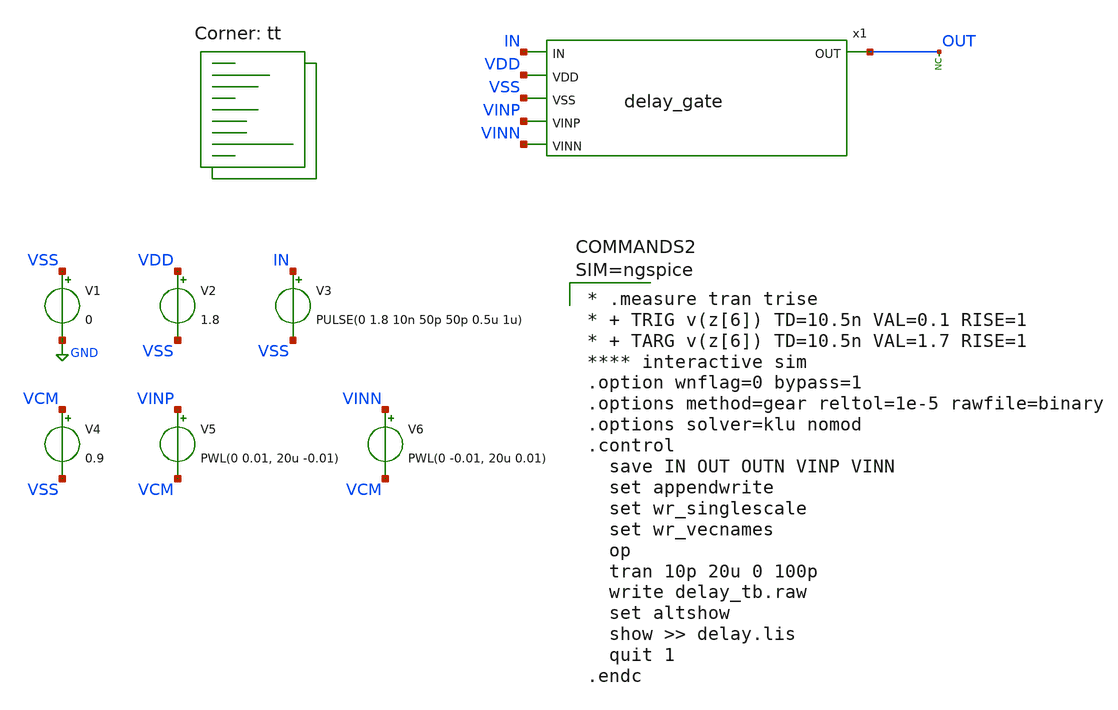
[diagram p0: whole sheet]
** sch_path: xschem/delay_tb.sch
.include $::SKYWATER_STDCELLS/sky130_fd_sc_hd.spice
**.subckt delay_tb
x1 IN VDD VSS VINP VINN OUT delay_gate
V1 VSS GND 0
V2 VDD VSS 1.8
V3 IN VSS PULSE(0 1.8 10n 50p 50p 0.5u 1u)
V4 VCM VSS 0.9
V5 VINP VCM PWL(0 0.01, 20u -0.01)
V6 VINN VCM PWL(0 -0.01, 20u 0.01)
* noconn OUT
**** begin user architecture code
.lib $::SKYWATER_MODELS/sky130.lib.spice tt


* .measure tran trise
* + TRIG v(z[6]) TD=10.5n VAL=0.1 RISE=1
* + TARG v(z[6]) TD=10.5n VAL=1.7 RISE=1
**** interactive sim
.option wnflag=0 bypass=1
.options method=gear reltol=1e-5 rawfile=binary
.options solver=klu nomod
.control
  save IN OUT OUTN VINP VINN
  set appendwrite
  set wr_singlescale
  set wr_vecnames
  op
  tran 10p 20u 0 100p
  write delay_tb.raw
  set altshow
  show >> delay.lis
  quit 1
.endc



**** end user architecture code
**.ends

* expanding   symbol:  delay_gate.sym # of pins=6
** sym_path: xschem/delay_gate.sym
** sch_path: xschem/delay_gate.sch
.subckt delay_gate IN VDD VSS VINP VINN OUT
*.ipin VINP
*.ipin VINN
*.ipin IN
*.ipin VSS
*.ipin VDD
*.opin OUT
XM1 net3 VINP net8 VDD sky130_fd_pr__pfet_01v8 L=1 W=3 nf=1 ad='int((nf+1)/2) * W/nf * 0.29' as='int((nf+2)/2) * W/nf * 0.29'
+ pd='2*int((nf+1)/2) * (W/nf + 0.29)' ps='2*int((nf+2)/2) * (W/nf + 0.29)' nrd='0.29 / W' nrs='0.29 / W'
+ sa=0 sb=0 sd=0 mult=1 m=1
XM2 net2 net1 net3 VDD sky130_fd_pr__pfet_01v8 L=1 W=3 nf=1 ad='int((nf+1)/2) * W/nf * 0.29' as='int((nf+2)/2) * W/nf * 0.29'
+ pd='2*int((nf+1)/2) * (W/nf + 0.29)' ps='2*int((nf+2)/2) * (W/nf + 0.29)' nrd='0.29 / W' nrs='0.29 / W'
+ sa=0 sb=0 sd=0 mult=1 m=1
XM3 net2 net1 net6 VSS sky130_fd_pr__nfet_01v8 L=1 W=1 nf=1 ad='int((nf+1)/2) * W/nf * 0.29' as='int((nf+2)/2) * W/nf * 0.29'
+ pd='2*int((nf+1)/2) * (W/nf + 0.29)' ps='2*int((nf+2)/2) * (W/nf + 0.29)' nrd='0.29 / W' nrs='0.29 / W'
+ sa=0 sb=0 sd=0 mult=1 m=1
XM4 net1 IN net5 VDD sky130_fd_pr__pfet_01v8 L=1 W=3 nf=1 ad='int((nf+1)/2) * W/nf * 0.29' as='int((nf+2)/2) * W/nf * 0.29'
+ pd='2*int((nf+1)/2) * (W/nf + 0.29)' ps='2*int((nf+2)/2) * (W/nf + 0.29)' nrd='0.29 / W' nrs='0.29 / W'
+ sa=0 sb=0 sd=0 mult=1 m=1
XM5 net1 IN net4 VSS sky130_fd_pr__nfet_01v8 L=1 W=1 nf=1 ad='int((nf+1)/2) * W/nf * 0.29' as='int((nf+2)/2) * W/nf * 0.29'
+ pd='2*int((nf+1)/2) * (W/nf + 0.29)' ps='2*int((nf+2)/2) * (W/nf + 0.29)' nrd='0.29 / W' nrs='0.29 / W'
+ sa=0 sb=0 sd=0 mult=1 m=1
XM6 net4 VINN net7 VSS sky130_fd_pr__nfet_01v8 L=1 W=1 nf=1 ad='int((nf+1)/2) * W/nf * 0.29' as='int((nf+2)/2) * W/nf * 0.29'
+ pd='2*int((nf+1)/2) * (W/nf + 0.29)' ps='2*int((nf+2)/2) * (W/nf + 0.29)' nrd='0.29 / W' nrs='0.29 / W'
+ sa=0 sb=0 sd=0 mult=1 m=1
x6 net2 VSS VSS VDD VDD OUT sky130_fd_sc_hd__buf_4
XM7 net5 VSS VDD VDD sky130_fd_pr__pfet_01v8 L=1 W=3 nf=1 ad='int((nf+1)/2) * W/nf * 0.29' as='int((nf+2)/2) * W/nf * 0.29'
+ pd='2*int((nf+1)/2) * (W/nf + 0.29)' ps='2*int((nf+2)/2) * (W/nf + 0.29)' nrd='0.29 / W' nrs='0.29 / W'
+ sa=0 sb=0 sd=0 mult=1 m=1
XM8 net6 VDD VSS VSS sky130_fd_pr__nfet_01v8 L=1 W=1 nf=1 ad='int((nf+1)/2) * W/nf * 0.29' as='int((nf+2)/2) * W/nf * 0.29'
+ pd='2*int((nf+1)/2) * (W/nf + 0.29)' ps='2*int((nf+2)/2) * (W/nf + 0.29)' nrd='0.29 / W' nrs='0.29 / W'
+ sa=0 sb=0 sd=0 mult=1 m=1
XM9 net7 VDD VSS VSS sky130_fd_pr__nfet_01v8 L=1 W=1 nf=1 ad='int((nf+1)/2) * W/nf * 0.29' as='int((nf+2)/2) * W/nf * 0.29'
+ pd='2*int((nf+1)/2) * (W/nf + 0.29)' ps='2*int((nf+2)/2) * (W/nf + 0.29)' nrd='0.29 / W' nrs='0.29 / W'
+ sa=0 sb=0 sd=0 mult=1 m=1
XM10 net8 VSS VDD VDD sky130_fd_pr__pfet_01v8 L=1 W=3 nf=1 ad='int((nf+1)/2) * W/nf * 0.29' as='int((nf+2)/2) * W/nf * 0.29'
+ pd='2*int((nf+1)/2) * (W/nf + 0.29)' ps='2*int((nf+2)/2) * (W/nf + 0.29)' nrd='0.29 / W' nrs='0.29 / W'
+ sa=0 sb=0 sd=0 mult=1 m=1
.ends

.GLOBAL GND
.end
